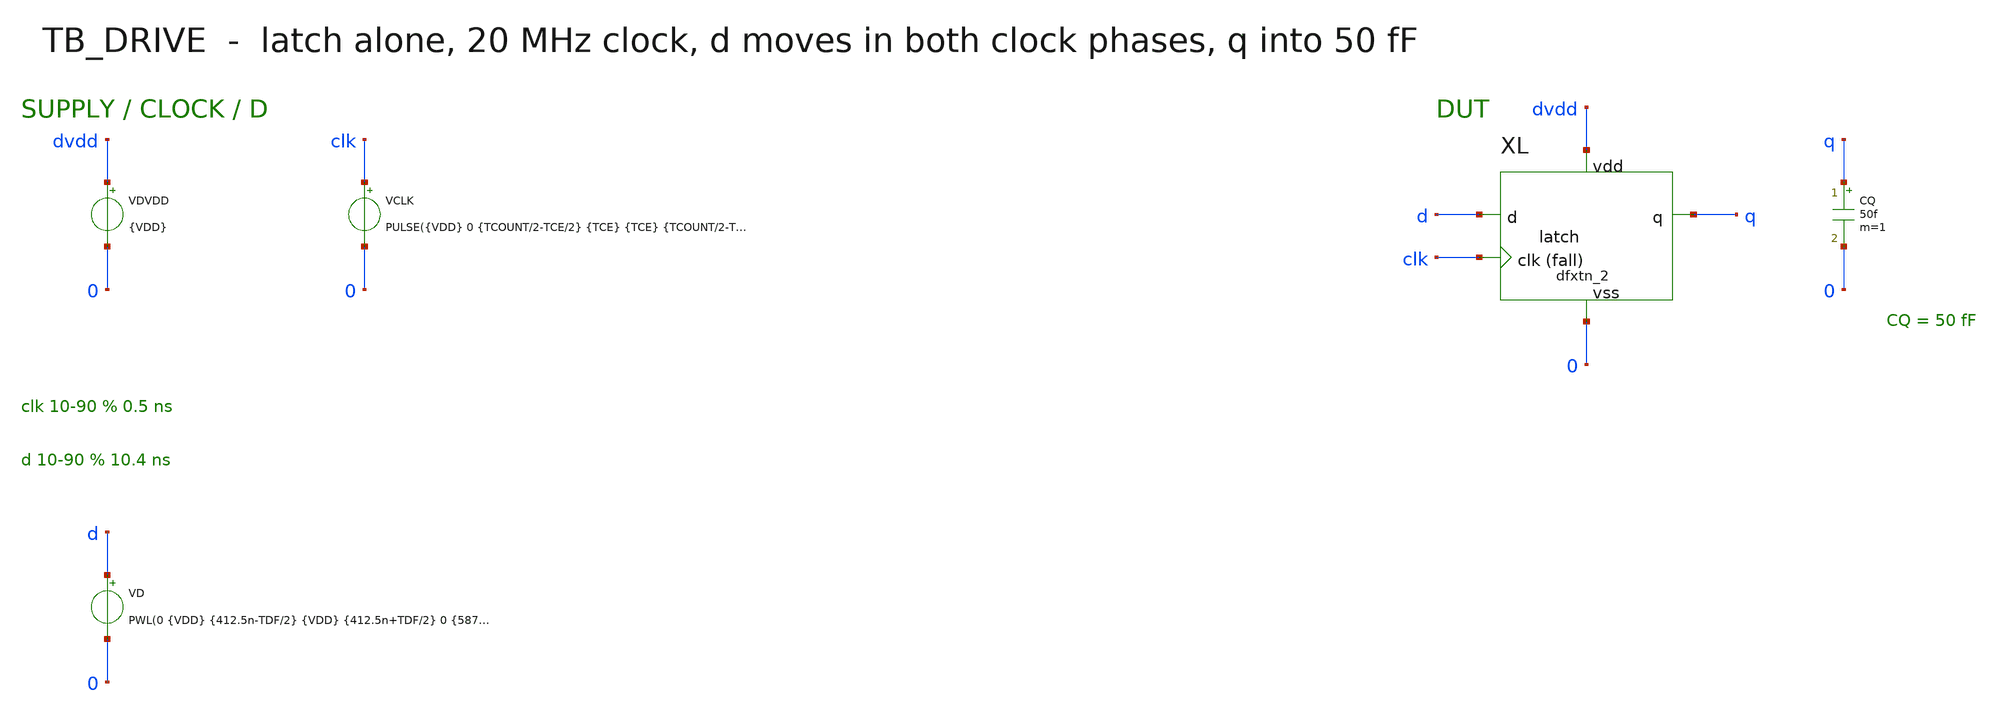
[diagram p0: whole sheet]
** sch_path: mixed_signal/latch/tb_drive.sch
**.subckt tb_drive
VDVDD dvdd 0 {VDD}
VCLK clk 0 PULSE({VDD} 0 {TCOUNT/2-TCE/2} {TCE} {TCE} {TCOUNT/2-TCE} {TCOUNT})
VD d 0 PWL(0 {VDD} {412.5n-TDF/2} {VDD} {412.5n+TDF/2} 0 {587.5n-TDF/2} 0 {587.5n+TDF/2} {VDD} {787.5n-TDF/2}
+ {VDD} {787.5n+TDF/2} 0 {962.5n-TDF/2} 0 {962.5n+TDF/2} {VDD})
XL d clk q dvdd 0 latch
CQ q 0 50f m=1
**** begin user architecture code

.include /foss/pdks/gf180mcuD/libs.tech/ngspice/design.ngspice
.lib /foss/pdks/gf180mcuD/libs.tech/ngspice/sm141064.ngspice typical
.include /foss/pdk_libs/gf180mcuD/libs.ref/gf180mcu_as_sc_mcu7t3v3/spice/gf180mcu_as_sc_mcu7t3v3.spice
.param VDD=3.3
.param TCOUNT=50n
.param TCE=6.250000e-10
.param TDF=1.300000e-08
.param TSTOP=1100n
.temp 27
.csparam cs_vdd={VDD}
.options savecurrents reltol=1e-4
.tran 5p {TSTOP} 0 20p
.control
run
let half = $&cs_vdd / 2
let hi90 = 0.9 * $&cs_vdd
let lo10 = 0.1 * $&cs_vdd
meas tran t_edge when v(clk)=$&half fall=1 td=413e-9
meas tran t_q when v(q)=$&half fall=1 td=100e-9
meas tran t_q90 when v(q)=$&hi90 fall=1 td=100e-9
meas tran t_q10 when v(q)=$&lo10 fall=1 td=100e-9
let tcq = t_q - t_edge
let q_fall = t_q10 - t_q90
set numdgt=10
echo RESULT_BEGIN
print tcq q_fall t_edge t_q
echo RESULT_END
quit
.endc

**** end user architecture code
**.ends

* expanding   symbol:  latch.sym # of pins=5
** sym_path: mixed_signal/latch/latch.sym
** sch_path: mixed_signal/latch/latch.sch
.subckt latch d clk q vdd vss
*.iopin vdd
*.iopin vss
*.ipin d
*.ipin clk
*.opin q
XFF vdd vdd vss vss clk d q gf180mcu_as_sc_mcu7t3v3__dfxtn_2
.ends

.end
